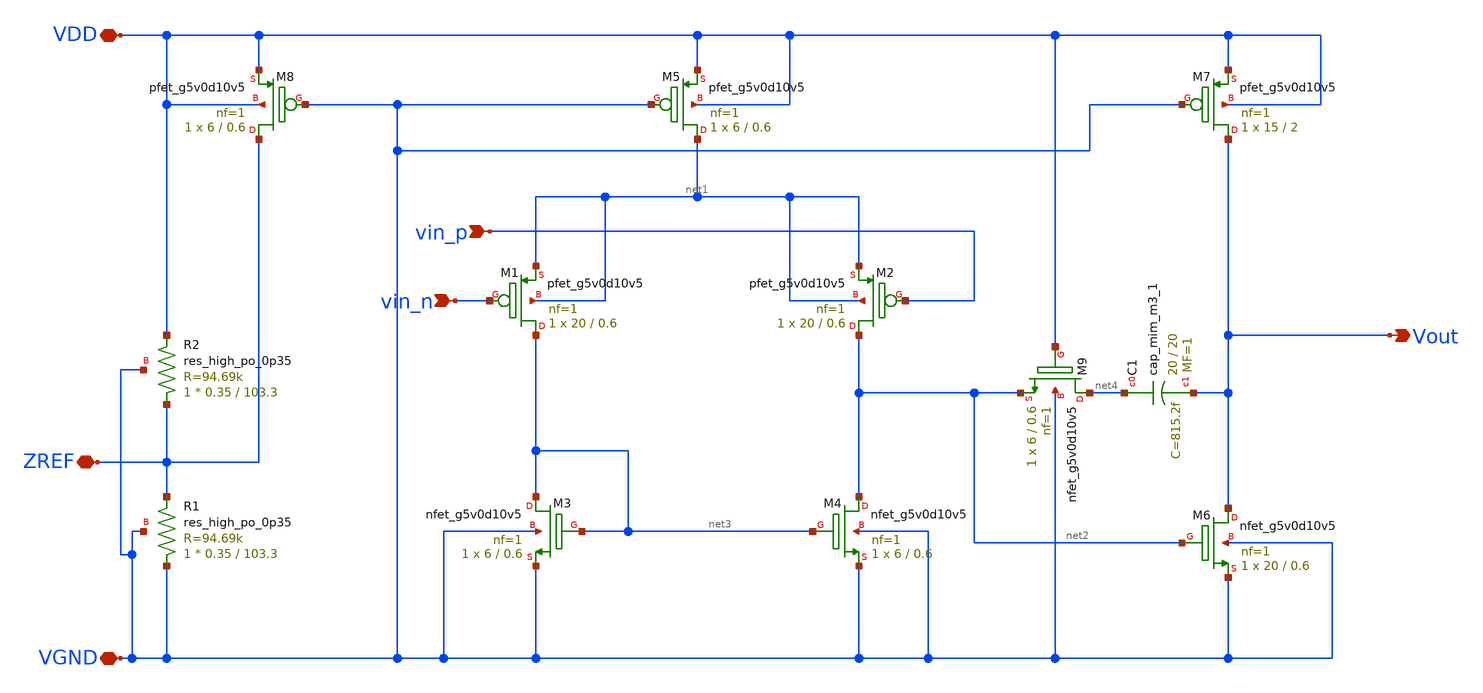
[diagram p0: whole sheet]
** sch_path: schematic/xschem/opamp.sch
**.subckt opamp vin_n vin_p Vout VDD ZREF VGND
*.ipin vin_n
*.ipin vin_p
*.opin Vout
*.iopin VDD
*.iopin ZREF
*.iopin VGND
XC1 net4 Vout sky130_fd_pr__cap_mim_m3_1 W=20 L=20 MF=1 m=1
XM4 net2 net3 VGND VGND sky130_fd_pr__nfet_g5v0d10v5 L=0.6 W=6 nf=1 ad='int((nf+1)/2) * W/nf * 0.29'
+ as='int((nf+2)/2) * W/nf * 0.29' pd='2*int((nf+1)/2) * (W/nf + 0.29)' ps='2*int((nf+2)/2) * (W/nf + 0.29)'
+ nrd='0.29 / W' nrs='0.29 / W' sa=0 sb=0 sd=0 mult=1 m=1
XM8 ZREF VGND VDD VDD sky130_fd_pr__pfet_g5v0d10v5 L=0.6 W=6 nf=1 ad='int((nf+1)/2) * W/nf * 0.29' as='int((nf+2)/2) * W/nf * 0.29'
+ pd='2*int((nf+1)/2) * (W/nf + 0.29)' ps='2*int((nf+2)/2) * (W/nf + 0.29)' nrd='0.29 / W' nrs='0.29 / W'
+ sa=0 sb=0 sd=0 mult=1 m=1
XM5 net1 VGND VDD VDD sky130_fd_pr__pfet_g5v0d10v5 L=0.6 W=6 nf=1 ad='int((nf+1)/2) * W/nf * 0.29' as='int((nf+2)/2) * W/nf * 0.29'
+ pd='2*int((nf+1)/2) * (W/nf + 0.29)' ps='2*int((nf+2)/2) * (W/nf + 0.29)' nrd='0.29 / W' nrs='0.29 / W'
+ sa=0 sb=0 sd=0 mult=1 m=1
XM7 Vout VGND VDD VDD sky130_fd_pr__pfet_g5v0d10v5 L=2 W=15 nf=1 ad='int((nf+1)/2) * W/nf * 0.29' as='int((nf+2)/2) * W/nf * 0.29'
+ pd='2*int((nf+1)/2) * (W/nf + 0.29)' ps='2*int((nf+2)/2) * (W/nf + 0.29)' nrd='0.29 / W' nrs='0.29 / W'
+ sa=0 sb=0 sd=0 mult=1 m=1
XM1 net3 vin_n net1 net1 sky130_fd_pr__pfet_g5v0d10v5 L=0.6 W=20 nf=1 ad='int((nf+1)/2) * W/nf * 0.29'
+ as='int((nf+2)/2) * W/nf * 0.29' pd='2*int((nf+1)/2) * (W/nf + 0.29)' ps='2*int((nf+2)/2) * (W/nf + 0.29)'
+ nrd='0.29 / W' nrs='0.29 / W' sa=0 sb=0 sd=0 mult=1 m=1
XM2 net2 vin_p net1 net1 sky130_fd_pr__pfet_g5v0d10v5 L=0.6 W=20 nf=1 ad='int((nf+1)/2) * W/nf * 0.29'
+ as='int((nf+2)/2) * W/nf * 0.29' pd='2*int((nf+1)/2) * (W/nf + 0.29)' ps='2*int((nf+2)/2) * (W/nf + 0.29)'
+ nrd='0.29 / W' nrs='0.29 / W' sa=0 sb=0 sd=0 mult=1 m=1
XM3 net3 net3 VGND VGND sky130_fd_pr__nfet_g5v0d10v5 L=0.6 W=6 nf=1 ad='int((nf+1)/2) * W/nf * 0.29'
+ as='int((nf+2)/2) * W/nf * 0.29' pd='2*int((nf+1)/2) * (W/nf + 0.29)' ps='2*int((nf+2)/2) * (W/nf + 0.29)'
+ nrd='0.29 / W' nrs='0.29 / W' sa=0 sb=0 sd=0 mult=1 m=1
XM6 Vout net2 VGND VGND sky130_fd_pr__nfet_g5v0d10v5 L=0.6 W=20 nf=1 ad='int((nf+1)/2) * W/nf * 0.29'
+ as='int((nf+2)/2) * W/nf * 0.29' pd='2*int((nf+1)/2) * (W/nf + 0.29)' ps='2*int((nf+2)/2) * (W/nf + 0.29)'
+ nrd='0.29 / W' nrs='0.29 / W' sa=0 sb=0 sd=0 mult=1 m=1
XM9 net4 VDD net2 VGND sky130_fd_pr__nfet_g5v0d10v5 L=0.6 W=6 nf=1 ad='int((nf+1)/2) * W/nf * 0.29' as='int((nf+2)/2) * W/nf * 0.29'
+ pd='2*int((nf+1)/2) * (W/nf + 0.29)' ps='2*int((nf+2)/2) * (W/nf + 0.29)' nrd='0.29 / W' nrs='0.29 / W'
+ sa=0 sb=0 sd=0 mult=1 m=1
XR1 VGND ZREF VGND sky130_fd_pr__res_high_po_0p35 W=0.35 L=103.3 mult=1 m=1
XR2 ZREF VDD VGND sky130_fd_pr__res_high_po_0p35 W=0.35 L=103.3 mult=1 m=1
**.ends
.end
